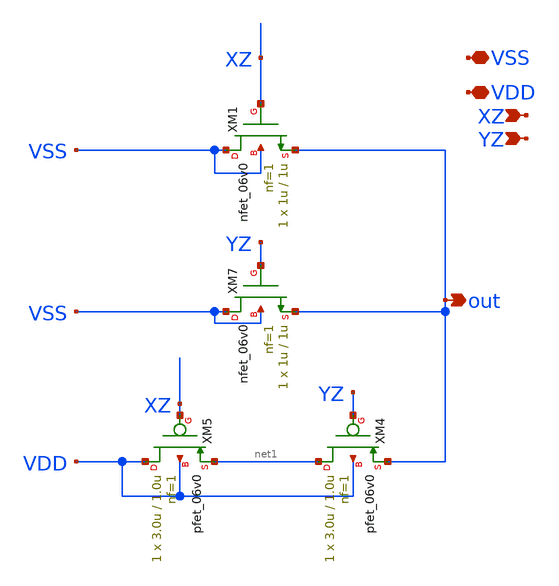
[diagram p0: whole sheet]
** sch_path: FINAL/XSCHEM/DECODER/Z.sch
**.subckt Z VSS VDD XZ YZ out
*.iopin VSS
*.iopin VDD
*.ipin XZ
*.ipin YZ
*.opin out
XM4 net1 YZ out VDD pfet_06v0 L=1.0u W=3.0u nf=1 ad='int((nf+1)/2) * W/nf * 0.18u' as='int((nf+2)/2) * W/nf * 0.18u'
+ pd='2*int((nf+1)/2) * (W/nf + 0.18u)' ps='2*int((nf+2)/2) * (W/nf + 0.18u)' nrd='0.18u / W' nrs='0.18u / W'
+ sa=0 sb=0 sd=0 m=1
XM5 VDD XZ net1 VDD pfet_06v0 L=1.0u W=3.0u nf=1 ad='int((nf+1)/2) * W/nf * 0.18u' as='int((nf+2)/2) * W/nf * 0.18u'
+ pd='2*int((nf+1)/2) * (W/nf + 0.18u)' ps='2*int((nf+2)/2) * (W/nf + 0.18u)' nrd='0.18u / W' nrs='0.18u / W'
+ sa=0 sb=0 sd=0 m=1
XM7 VSS YZ out VSS nfet_06v0 L=1u W=1u nf=1 ad='int((nf+1)/2) * W/nf * 0.18u' as='int((nf+2)/2) * W/nf * 0.18u'
+ pd='2*int((nf+1)/2) * (W/nf + 0.18u)' ps='2*int((nf+2)/2) * (W/nf + 0.18u)' nrd='0.18u / W' nrs='0.18u / W'
+ sa=0 sb=0 sd=0 m=1
XM1 VSS XZ out VSS nfet_06v0 L=1u W=1u nf=1 ad='int((nf+1)/2) * W/nf * 0.18u' as='int((nf+2)/2) * W/nf * 0.18u'
+ pd='2*int((nf+1)/2) * (W/nf + 0.18u)' ps='2*int((nf+2)/2) * (W/nf + 0.18u)' nrd='0.18u / W' nrs='0.18u / W'
+ sa=0 sb=0 sd=0 m=1
**.ends
.end
